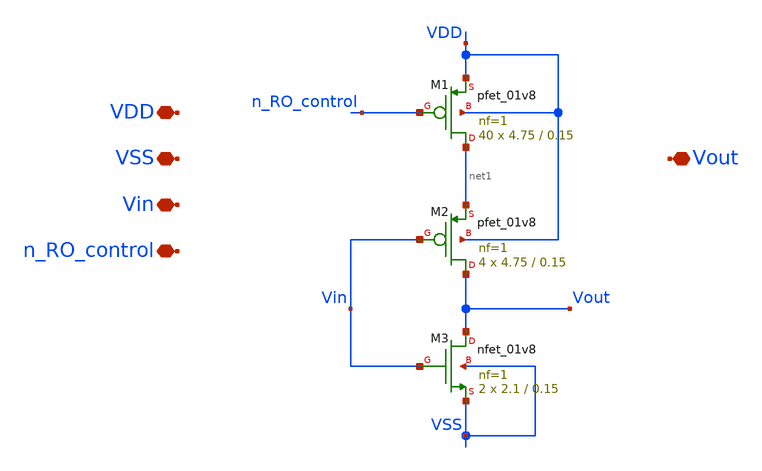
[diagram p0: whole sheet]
** sch_path: TT/inv1.sch
**.subckt inv1 VDD VSS Vin Vout n_RO_control
*.iopin VDD
*.iopin VSS
*.iopin Vin
*.iopin Vout
*.iopin n_RO_control
XM1 net1 n_RO_control VDD VDD sky130_fd_pr__pfet_01v8 L=0.15 W=4.75 nf=1 ad='int((nf+1)/2) * W/nf * 0.29'
+ as='int((nf+2)/2) * W/nf * 0.29' pd='2*int((nf+1)/2) * (W/nf + 0.29)' ps='2*int((nf+2)/2) * (W/nf + 0.29)'
+ nrd='0.29 / W' nrs='0.29 / W' sa=0 sb=0 sd=0 mult=40 m=40
XM2 Vout Vin net1 VDD sky130_fd_pr__pfet_01v8 L=0.15 W=4.75 nf=1 ad='int((nf+1)/2) * W/nf * 0.29' as='int((nf+2)/2) * W/nf * 0.29'
+ pd='2*int((nf+1)/2) * (W/nf + 0.29)' ps='2*int((nf+2)/2) * (W/nf + 0.29)' nrd='0.29 / W' nrs='0.29 / W'
+ sa=0 sb=0 sd=0 mult=4 m=4
XM3 Vout Vin VSS VSS sky130_fd_pr__nfet_01v8 L=0.15 W=2.1 nf=1 ad='int((nf+1)/2) * W/nf * 0.29' as='int((nf+2)/2) * W/nf * 0.29'
+ pd='2*int((nf+1)/2) * (W/nf + 0.29)' ps='2*int((nf+2)/2) * (W/nf + 0.29)' nrd='0.29 / W' nrs='0.29 / W'
+ sa=0 sb=0 sd=0 mult=2 m=2
**.ends
.end
